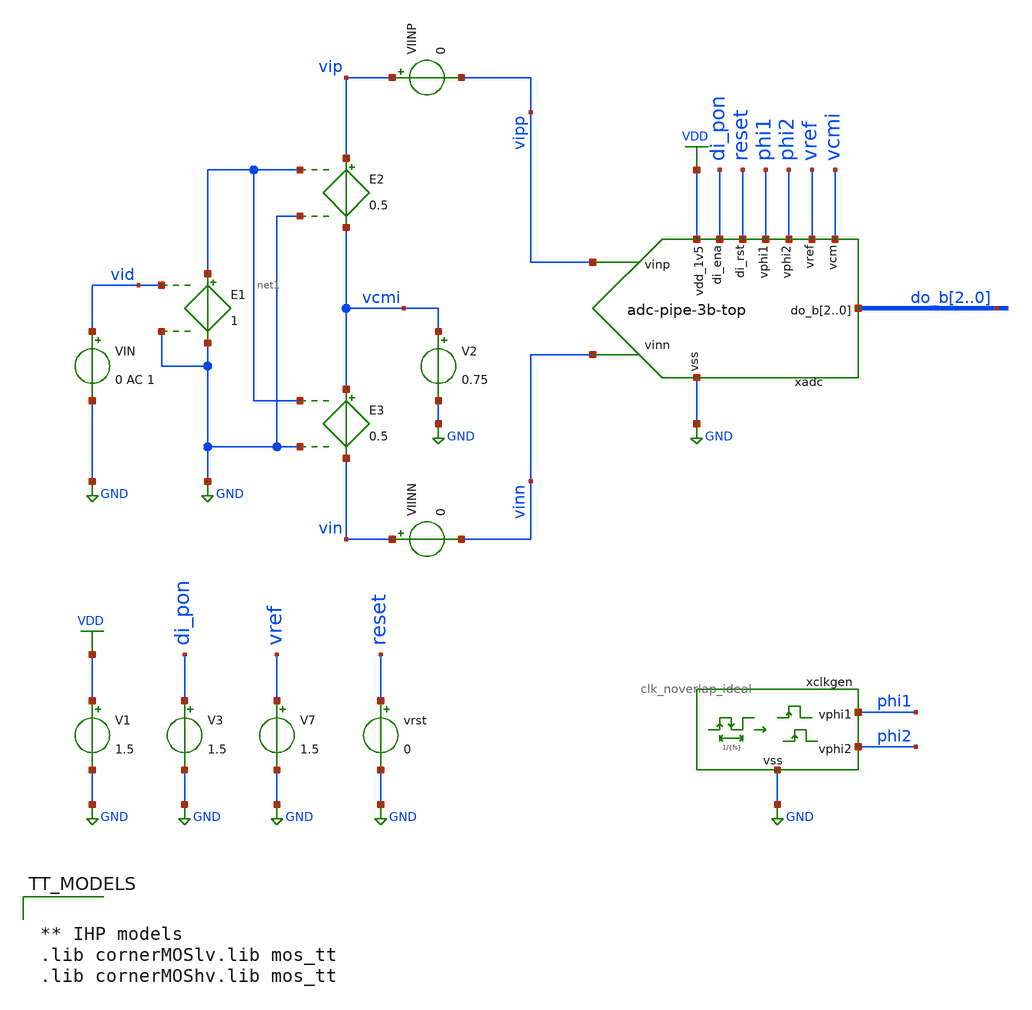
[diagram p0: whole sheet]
** sch_path: xschem/adc-pipe-3b-top_tb.sch
* xschem/ota-5t-fd.sch:
* (c) 2025 M. Koefinger
**.subckt adc-pipe-3b-top_tb
V1 VDD GND 1.5
V3 di_pon GND 1.5
V2 vcmi GND 0.75
E3 vcmi vin net1 GND 0.5
E2 vip vcmi net1 GND 0.5
VIN vid GND 0 AC 1
E1 net1 GND vid GND 1
VIINP vip vipp 0
VIINN vin vinn 0
xclkgen phi1 phi2 GND clk_noverlap_ideal fs={fs} tnover=50n tdelay=0 trf=5n
V7 vref GND 1.5
vrst reset GND 0
xadc vcmi vref phi2 phi1 reset di_pon VDD vipp do_b2 do_b1 do_b0 vinn GND adc-pipe-3b-top
**** begin user architecture code


.include ../xspice/adc_pipe_encoder_TOP/adc_pipe_encoder_TOP.xspice
.include adc-pipe-3b-top_tb.save
.options savecurrents
.options method=gear reltol=1e-4
.options sparse
.param fs=2Meg
.param ibias=1.5u
.param cap=100f
.param cap_load = 100f
.param ron=1
.param roff=1G

.control
save vin vip vid vcmi phi1 phi2 vref clock reset do_b2 do_b1 do_b0 vdig vdig_plt
save xadc.xpipe.vres1p xadc.xpipe.vres1n xadc.xpipe.vres2p xadc.xpipe.vres2n
save xadc.xpipe.xmdac1.vdac_p xadc.xpipe.xmdac1.vdac_n xadc.xpipe.xmdac1.vgndp
+ xadc.xpipe.xmdac1.vgndn xadc.xpipe.xmdac1.vfb xadc.xpipe.xmdac1.vbp
save xadc.xpipe.xmdac1.xc1.vc_p xadc.xpipe.xmdac1.xc2.vc_p xadc.xpipe.xmdac1.xc3.vc_p
+ xadc.xpipe.xmdac1.xc4.vc_p
save xadc.xpipe.xmdac2.vdac_p xadc.xpipe.xmdac2.vdac_n xadc.xpipe.xmdac2.vgndp
+ xadc.xpipe.xmdac2.vgndn xadc.xpipe.xmdac2.vfb xadc.xpipe.xmdac2.vbp
save xadc.xpipe.xmdac2.xc1.vc_p xadc.xpipe.xmdac2.xc2.vc_p xadc.xpipe.xmdac2.xc3.vc_p
+ xadc.xpipe.xmdac2.xc4.vc_p
save xadc.do3 xadc.do22 xadc.do21 xadc.do20 xadc.do12 xadc.do11 xadc.do10

set wr_singlescale
set wr_vecnames
option numdgt=3

** Sim Options
set opSimOnly = 0

** Set sampling frequency
let fs = 2Meg

** Set Startup time
let n_per_startup = 100
let t_delay = n_per_startup/fs

** Set input signal
let f_sig = 100k
let tper_sig = 1/f_sig
let tfr_sig = tper_sig*5/10
let ton_sig = tper_sig*1/1000

** Set transient simulation parameters
let tstep = 0.001/fs
let tstop = 2/f_sig+t_delay
let tstart = t_delay

alter @VIN[DC] = 0.0

** Main Simulations
if $opSimOnly eq 0
	** Set sources
	alter @VRST[PULSE] = [1.5 0 0 10p 10p $&t_delay)
	*alter @VIN[PULSE]=[ -1.5 1.5 0 $&tfr_sig $&tfr_sig $&ton_sig $&tper_sig 0 ]
	alter @VIN[SIN] = [ 0 1 $&f_sig t_delay 0 0 ]
	tran $&tstep $&tstop $&tstart

	setplot tran1
	let vid = v(vid)
	let vres1 = xadc.xpipe.vres1p - xadc.xpipe.vres1n
	let vres2 = xadc.xpipe.vres2p - xadc.xpipe.vres2n

	let vcmo1 = (xadc.xpipe.vres1p+xadc.xpipe.vres1n)/2
	let vcmo2 = (xadc.xpipe.vres2p+xadc.xpipe.vres2n)/2
	let vcmi1 = (xadc.xpipe.xmdac1.vgndp+xadc.xpipe.xmdac1.vgndn)/2
	let vcmi2 = (xadc.xpipe.xmdac2.vgndp+xadc.xpipe.xmdac2.vgndn)/2

	let vcap_in_n = v(xadc.xpipe.xmdac1.xc2.vc_p,xadc.xpipe.xmdac1.vgndn)
	let v_in_n = v(vin,vcmi1)
	let v_dac_p = v(xadc.xpipe.xmdac1.vdac_p,vcmi1)
	let vcap_in_p = v(xadc.xpipe.xmdac1.xc4.vc_p,xadc.xpipe.xmdac1.vgndp)
	let v_in_p = v(vip,vcmi)
	let v_dac_n = v(xadc.xpipe.xmdac1.vdac_n,vcmi1)

	let err1 = 2*vid-vres1
	let err2 = 2*vres1-vres2

	let vdac_1 = v(xadc.xpipe.xmdac1.vdac_p,xadc.xpipe.xmdac1.vdac_n)
	let vdac_2 = v(xadc.xpipe.xmdac2.vdac_p,xadc.xpipe.xmdac2.vdac_n)

	let clock = phi1
	let reset = reset
	let do_b2 = do_b2
	let do_b1 = do_b1
	let do_b0 = do_b0
	let vdig = do_b2*4 + do_b1*2 + do_b0
	meas tran vdig_max max vdig
	let vdig_plt = 2*(vdig/vdig_max-0.5)

	write adc-pipe-3b-top_tb.raw

	*plot vid vres1 vcmo1 vcmi1 phi2
	*plot vcap_in_n v_in_n v_dac_p vcap_in_p v_in_p
	*plot err1
	*plot err2
	*plot vid vres1 vres2
	plot xadc.do12 xadc.do11 xadc.do10 vid
	plot xadc.do22 xadc.do21 xadc.do20 vres1
	plot xadc.do3 vres2
	plot do_b2 do_b1 do_b0
	*plot vid vdig_plt
	plot vid vdac_1 vres1
	plot vres1 vdac_2 vres2
end

set appendwrite

alter @VIN[DC] = 0
optran 0 0 0 0.1u $&t_delay 0
op
remzerovec
write adc-pipe-3b-top_tb.raw

.endc



** IHP models
.lib cornerMOSlv.lib mos_tt
.lib cornerMOShv.lib mos_tt


**** end user architecture code
**.ends

* expanding   symbol:  clk_noverlap_ideal.sym # of pins=3
** sym_path: xschem/clk_noverlap_ideal.sym
** sch_path: xschem/clk_noverlap_ideal.sch
.subckt clk_noverlap_ideal vphi1 vphi2 vss  fs=100Meg tnover=2n tdelay=0 trf=0.1n
*.iopin vss
*.opin vphi1
*.opin vphi2
V1 vphi1 vss 0 PULSE 0 1.5 {tdelay} {trf} {trf} {0.5/{fs}-{tnover}} {1/{fs}} 0
V2 vphi2 vss 0 PULSE 0 1.5 {{tdelay}+{0.5/{fs}}} {trf} {trf} {0.5/{fs}-{tnover}} {1/{fs}} 0
.ends


* expanding   symbol:  adc-pipe-3b-top.sym # of pins=11
** sym_path: xschem/adc-pipe-3b-top.sym
** sch_path: xschem/adc-pipe-3b-top.sch
.subckt adc-pipe-3b-top vcm vref vphi2 vphi1 di_rst di_ena vdd_1v5 vinp do_b2 do_b1 do_b0 vinn vss
*.ipin vinp
*.ipin vinn
*.ipin di_rst
*.ipin di_ena
*.ipin vphi1
*.ipin vphi2
*.ipin vref
*.ipin vcm
*.iopin vdd_1v5
*.iopin vss
*.opin do_b2,do_b1,do_b0
xpipe di_ena vphi2 vphi1 vcm vref vdd_1v5 vinp vinn do3 do22 do21 do20 do12 do11 do10 vss
+ adc-pipe-3b-core
ADUT [ vphi1 vphi2 di_rst do12 do11 do10 do22 do21 do20 do3 ] [ do_b2 do_b1 do_b0 ] encoder
.ends


* expanding   symbol:  adc-pipe-3b-core.sym # of pins=12
** sym_path: xschem/adc-pipe-3b-core.sym
** sch_path: xschem/adc-pipe-3b-core.sch
.subckt adc-pipe-3b-core di_ena vphi2 vphi1 vcm vref vdd_1v5 vinp vinn do3 do22 do21 do20 do12 do11
+ do10 vss
*.iopin vdd_1v5
*.ipin vref
*.ipin vcm
*.ipin vphi1
*.ipin vphi2
*.ipin vinp
*.ipin vinn
*.iopin vss
*.ipin di_ena
*.opin do12,do11,do10
*.opin do22,do21,do20
*.opin do3
xmdac1 vdd_1v5 net1 vphi1 vphi2 vinp do12 do11 do10 vcm vss vres1p vcm vres1n vinn di_ena vss
+ mdac-tri-lvl
xadc1 do12 do11 do10 vinp vinn vref vcm vphi2 vss vphi1 adc-tri-lvl-ideal
xmdac2 vdd_1v5 net2 vphi2 vphi1 vres1p do22 do21 do20 vcm vss vres2p vcm vres2n vres1n di_ena vss
+ mdac-tri-lvl
xadc2 do22 do21 do20 vres1p vres1n vref vcm vphi1 vss vphi2 adc-tri-lvl-ideal
I0 vdd_1v5 net1 1.5u
I1 vdd_1v5 net2 1.5u
xadc3 do3 vres2p vres2n vcm vphi2 vss net3 vdd_1v5 vphi1 adc-1b-ideal
.ends


* expanding   symbol:  mdac-tri-lvl.sym # of pins=14
** sym_path: xschem/mdac-tri-lvl.sym
** sch_path: xschem/mdac-tri-lvl.sch
.subckt mdac-tri-lvl vdd_1v5 ibias_1u5 vhold vtrack vi_p di_code2 di_code1 di_code0 vref_p vref_n
+ vo_p vcm vo_n vi_n di_ena vss
*.ipin vi_p
*.ipin vi_n
*.ipin di_ena
*.iopin vss
*.iopin vdd_1v5
*.ipin ibias_1u5
*.opin vo_n
*.opin vo_p
*.ipin vref_p
*.ipin vref_n
*.ipin vcm
*.ipin di_code2,di_code1,di_code0
*.ipin vtrack
*.ipin vhold
xota vdd_1v5 vfb vo_p vo_n vgndp vgndn ibias_1u5 di_ena vss vbp ota-5t-fd
S1 vgndn vo_p vtrack vss SW1
xcmfb vhold vtrack vss vo_p vcm vbp vfb vo_n cmfb_sc cap={cap} div=10
S2 vgndp vo_n vtrack vss SW1
xc1 vhold vo_p vgndn vi_p vtrack vss sw_cap cap={cap} ron=1 roff=1G
xc2 vhold vdac_n vgndn vi_p vtrack vss sw_cap cap={cap} ron=1 roff=1G
xc3 vhold vo_n vgndp vi_n vtrack vss sw_cap cap={cap} ron=1 roff=1G
xc4 vhold vdac_p vgndp vi_n vtrack vss sw_cap cap={cap} ron=1 roff=1G
xsw1 di_code2 di_code1 di_code0 vref_p vref_n vdac_n vcm vss sw_dac ron=1 roff=1G
xsw2 di_code2 di_code1 di_code0 vref_n vref_p vdac_p vcm vss sw_dac ron=1 roff=1G
.ends


* expanding   symbol:  adc-tri-lvl-ideal.sym # of pins=8
** sym_path: xschem/adc-tri-lvl-ideal.sym
** sch_path: xschem/adc-tri-lvl-ideal.sch
.subckt adc-tri-lvl-ideal do[2] do[1] do[0] vip vin vref vcm vclk vss vclk_reg
*.iopin vss
*.ipin vip
*.ipin vin
*.ipin vref
*.ipin vcm
*.ipin vclk
*.opin do[2],do[1],do[0]
*.ipin vclk_reg
xcomp1 D1 vip vin vcm vref vss comp-macro
xcomp2 D0 vip vin vref vcm vss comp-macro
**** begin user architecture code


a31 Q_REG0 CLK_REG NULL NULL %d(Q0 NQ0) dff1
a32 Q_REG1 CLK_REG NULL NULL %d(Q1 NQ1) dff1


**** end user architecture code
**** begin user architecture code


.model adc_buf adc_bridge(in_low=0.7499 in_high=0.7501)
.model dac1 dac_bridge(out_low = 0 out_high = 1.5 out_undef = 0 input_load = 0.1e-15 t_rise =
+ 0.01e-9 t_fall = 0.01e-9)
.model inv1 d_inverter(rise_delay = 0.01e-9 fall_delay = 0.01e-9 input_load = 0.1e-15)
.model and1 d_and(rise_delay = 0.01e-9 fall_delay = 0.01e-9 input_load = 0.01e-15)
.model dff1 d_dff(clk_delay = 0.01e-9 set_delay = 0.01e-9 reset_delay = 0.01e-9 ic = 0 rise_delay =
+ 0.01e-9 fall_delay = 0.01e-9)
.model dlatch1 d_dlatch(data_delay = 0.01e-9 enable_delay = 0.01e-9 set_delay = 0.01e-9 reset_delay
+ = 0.01e-9 ic = 0 rise_delay = 0.01e-9 fall_delay = 0.01e-9)

**** end user architecture code
A1 [ vclk ] [ CLK ] adc_buf
A3 [ H1 ] [ do1 ] dac1
A4 [ H2 ] [ do2 ] dac1
**** begin user architecture code


a23 [NQ1 Q0] %d(H0) and1
a24 [NQ1 NQ0] %d(H1) and1
a25 [Q1 Q0] %d(H2) and1


**** end user architecture code
A2 [ H0 ] [ do0 ] dac1
V1 do2 do[2] 0
V2 do1 do[1] 0
V3 do0 do[0] 0
**** begin user architecture code


a21 D0 CLK NULL NULL %d(Q_REG0 NQ_REG0) dlatch1
a22 D1 CLK NULL NULL %d(Q_REG1 NQ_REG1) dlatch1


**** end user architecture code
A5 [ vclk_reg ] [ CLK_REG ] adc_buf
.ends


* expanding   symbol:  adc-1b-ideal.sym # of pins=9
** sym_path: xschem/legacy/adc-1b-ideal.sym
** sch_path: xschem/legacy/adc-1b-ideal.sch
.subckt adc-1b-ideal do vip vin vcm vclk vss do_b vdd vclk_reg
*.iopin vss
*.ipin vip
*.ipin vin
*.ipin vcm
*.ipin vclk
*.opin do_b
*.opin do
*.iopin vdd
*.ipin vclk_reg
**** begin user architecture code


.model adc_buf adc_bridge(in_low=0.7499 in_high=0.7501)
.model dac1 dac_bridge(out_low = 0 out_high = 1.5 out_undef = 0 input_load = 0.1e-15 t_rise =
+ 0.01e-9 t_fall = 0.01e-9)
.model nor1 d_nor(rise_delay = 0.01e-9 fall_delay = 0.01e-9 input_load = 0.01e-15)
.model dlatch1 d_dlatch(data_delay = 0.01e-9 enable_delay = 0.01e-9 set_delay = 0.01e-9 reset_delay
+ = 0.01e-9 ic = 0 rise_delay = 0.01e-9 fall_delay = 0.01e-9)
.model dff1 d_dff(clk_delay = 0.01e-9 set_delay = 0.01e-9 reset_delay = 0.01e-9 ic = 0 rise_delay =
+ 0.01e-9 fall_delay = 0.01e-9)


**** end user architecture code
A3 [ NQ1 ] [ do_b ] dac1
A2 [ Q1 ] [ do ] dac1
**** begin user architecture code


a21 [D0 NQ0] Q0 nor1
a22 [ND0 Q0] NQ0 nor1


**** end user architecture code
xcomp vdd vclk ND0 D0 vin vcm vcm vip vss sal-macro
**** begin user architecture code


a23 Q0 CLK NULL NULL %d(Q_REG0 NULL) dlatch1
a24 NQ0 CLK NULL NULL %d(NQ_REG0 NULL) dlatch1


**** end user architecture code
A1 [ vclk ] [ CLK ] adc_buf
**** begin user architecture code


a31 Q_REG0 CLK_REG NULL NULL %d(Q1 NULL) dff1
a32 NQ_REG0 CLK_REG NULL NULL %d(NQ1 NULL) dff1


**** end user architecture code
A4 [ vclk_reg ] [ CLK_REG ] adc_buf
.ends


* expanding   symbol:  ota-5t-fd.sym # of pins=10
** sym_path: xschem/ota-5t-fd.sym
** sch_path: xschem/ota-5t-fd.sch
.subckt ota-5t-fd vdd vfb voutp voutn vinp vinn ibias_1u5 d_ena vss vbp
*.ipin ibias_1u5
*.iopin vdd
*.iopin vss
*.ipin vinp
*.ipin vinn
*.opin voutn
*.ipin d_ena
*.opin voutp
*.ipin vfb
*.opin vbp
XMN3 tail gate_n vss vss sg13_lv_nmos w=2.5u l=0.5u ng=5 m=1 mm_ok=1
XMP2 voutp vfb vdd vdd sg13_lv_pmos w=0.5u l=0.5u ng=1 m=1 mm_ok=1
XMN1 voutn vinp tail vss sg13_lv_nmos w=5.5u l=0.5u ng=11 m=1 mm_ok=1
XMN2 voutp vinn tail vss sg13_lv_nmos w=5.5u l=0.5u ng=11 m=1 mm_ok=1
XMP1 voutn vfb vdd vdd sg13_lv_pmos w=0.5u l=0.5u ng=1 m=1 mm_ok=1
XMN4 ibias_1u5 gate_n vss vss sg13_lv_nmos w=1.5u l=0.5u ng=3 m=1 mm_ok=1
XMN5 gate_n ena_n vss vss sg13_lv_nmos w=0.5u l=0.13u ng=1 m=1 mm_ok=1
XMPSW1 vfb ena vdd vdd sg13_lv_pmos w=1.5u l=0.13u ng=1 m=1 mm_ok=1
XMN8 ena ena_n vss vss sg13_lv_nmos w=0.5u l=0.13u ng=1 m=1 mm_ok=1
XMP5 ena ena_n vdd vdd sg13_lv_pmos w=1.5u l=0.13u ng=1 m=1 mm_ok=1
XMN6 ibias_1u5 ena gate_n vss sg13_lv_nmos w=0.5u l=0.13u ng=1 m=1 mm_ok=1
XMN7 ena_n d_ena vss vss sg13_lv_nmos w=0.5u l=0.13u ng=1 m=1 mm_ok=1
XMP4 ena_n d_ena vdd vdd sg13_lv_pmos w=1.5u l=0.13u ng=1 m=1 mm_ok=1
XMN9 vbp gate_n vss vss sg13_lv_nmos w=1u l=0.5u ng=2 m=1 mm_ok=1
XMP3 vbp vbp vdd vdd sg13_lv_pmos w=0.5u l=0.5u ng=1 m=1 mm_ok=1
.ends


* expanding   symbol:  cmfb_sc.sym # of pins=8
** sym_path: xschem/cmfb_sc.sym
** sch_path: xschem/cmfb_sc.sch
.subckt cmfb_sc vphi2 vphi1 vss vo_p vcm vbias vfb vo_n  cap=100f div=10
*.ipin vcm
*.ipin vphi2
*.ipin vphi1
*.iopin vss
*.ipin vbias
*.iopin vo_p
*.iopin vo_n
*.opin vfb
C1 vo_p vfb 100f m=1
C2 net1 net2 10f m=1
C3 vfb vo_n 100f m=1
C4 net2 net3 10f m=1
S3 net1 vo_p vphi1 vss SW1
S4 vcm net1 vphi2 vss SW1
S6 net2 vfb vphi1 vss SW1
S7 vbias net2 vphi2 vss SW1
S9 net3 vo_n vphi1 vss SW1
S10 vcm net3 vphi2 vss SW1
.ends


* expanding   symbol:  sw_cap.sym # of pins=6
** sym_path: xschem/sw_cap.sym
** sch_path: xschem/sw_cap.sch
.subckt sw_cap di_1 vi1 vo vi2 di_2 vss  cap=100f ron=1 roff=1G
*.ipin di_1
*.ipin di_2
*.iopin vi1
*.iopin vi2
*.iopin vo
*.iopin vss
C1 vc_p vo {cap} m=1
S1 vi1 vc_p di_1 vss SW1
S2 vi2 vc_p di_2 vss SW1
.ends


* expanding   symbol:  sw_dac.sym # of pins=6
** sym_path: xschem/sw_dac.sym
** sch_path: xschem/sw_dac.sch
.subckt sw_dac di_code2 di_code1 di_code0 vref_p vref_n vo vcm vss  ron=1 roff=1G
*.ipin di_code2,di_code1,di_code0
*.iopin vref_p
*.iopin vref_n
*.iopin vo
*.iopin vss
*.iopin vcm
S1 vref_p vo di_code2 vss SW1
S2 vref_n vo di_code1 vss SW1
S3 vcm vo di_code0 vss SW1
.ends


* expanding   symbol:  comp-macro.sym # of pins=6
** sym_path: xschem/comp-macro.sym
** sch_path: xschem/comp-macro.sch
.subckt comp-macro do vip_1 vin_1 vip_2 vin_2 vss
*.iopin vss
*.ipin vip_1
*.ipin vin_1
*.ipin vip_2
*.ipin vin_2
*.opin do
A1 [ net1 ] [ do ] comp0
E1 net1 net2 vip_1 vin_1 1
E2 net2 vss vip_2 vin_2 1
**** begin user architecture code

.model comp0 adc_bridge(in_low=-0.0001 in_high=0.0001)

**** end user architecture code
.ends


* expanding   symbol:  sal-macro.sym # of pins=9
** sym_path: xschem/sal-macro.sym
** sch_path: xschem/sal-macro.sch
.subckt sal-macro vdd vclk do_b do vin_1 vip_2 vin_2 vip_1 vss
*.iopin vss
*.ipin vip_1
*.ipin vip_2
*.ipin vin_2
*.opin do
*.ipin vin_1
*.iopin vdd
*.opin do_b
*.ipin vclk
A1 [ net5 ] [ do ] comp0
G1 net2 net1 vip_1 net1 10e-6
**** begin user architecture code

.model comp0 adc_bridge(in_low=0.74 in_high=0.76)

**** end user architecture code
G3 net3 net1 vin_1 net1 10e-6
S1 net1 vss vclk vss SW1
G2 net5 net3 net4 net3 10e-6
G4 net4 net2 net5 net2 10e-6
G5 vdd net5 vdd net4 10e-6
G6 vdd net4 vdd net5 10e-6
S3 vdd net4 vdd vclk SW1
S4 vdd net2 vdd vclk SW1
S5 vdd net5 vdd vclk SW1
S6 vdd net2 vdd vclk SW1
A2 [ net4 ] [ do_b ] comp0
R1 vdd net4 1Meg m=1
R2 vdd net5 1Meg m=1
R3 net5 net3 1Meg m=1
R4 net4 net2 1Meg m=1
R5 net2 net1 100Meg m=1
R6 net3 net1 100e-6 m=1
.ends

.GLOBAL GND
.GLOBAL VDD
**** begin user architecture code
.MODEL SW1 SW( VT=0.75 VH=0.01 RON=1 ROFF=100Meg )
.model encoder d_cosim simulation="/foss/designs/verilog/rtl/adc_pipe_encoder_TOP.so"
**** end user architecture code
.end
